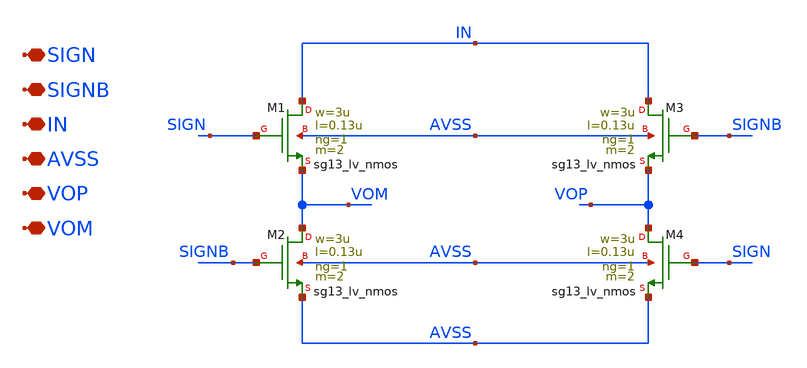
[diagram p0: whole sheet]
** sch_path: current_generator/analog/DAC/dsw.sch
**.subckt dsw SIGN SIGNB IN AVSS VOP VOM
*.iopin SIGN
*.iopin SIGNB
*.iopin IN
*.iopin AVSS
*.iopin VOP
*.iopin VOM
XM1 IN SIGN VOM AVSS sg13_lv_nmos w=3u l=0.13u ng=1 m=2 mm_ok=1
XM2 VOM SIGNB AVSS AVSS sg13_lv_nmos w=3u l=0.13u ng=1 m=2 mm_ok=1
XM3 IN SIGNB VOP AVSS sg13_lv_nmos w=3u l=0.13u ng=1 m=2 mm_ok=1
XM4 VOP SIGN AVSS AVSS sg13_lv_nmos w=3u l=0.13u ng=1 m=2 mm_ok=1
**.ends
.end
